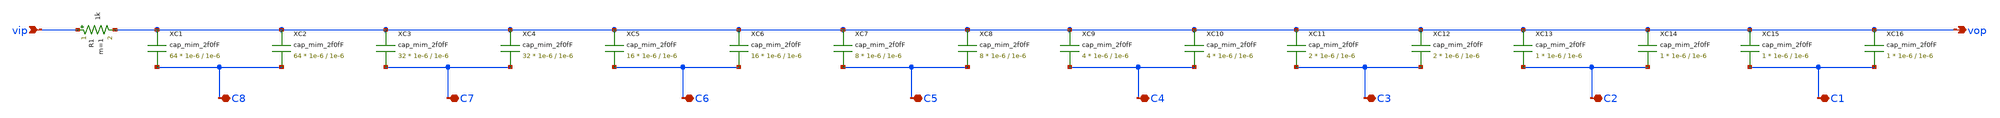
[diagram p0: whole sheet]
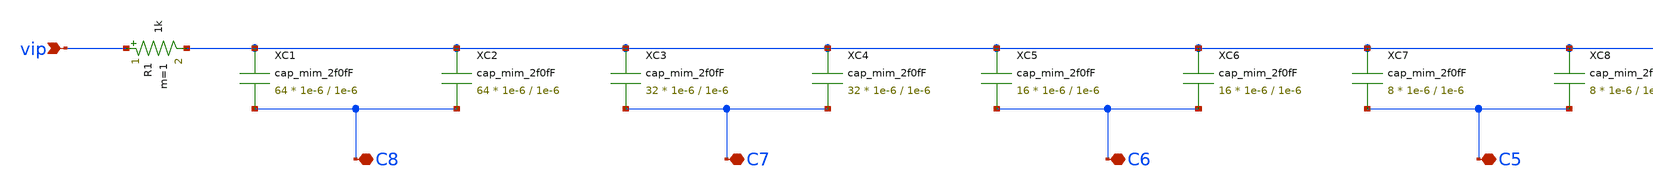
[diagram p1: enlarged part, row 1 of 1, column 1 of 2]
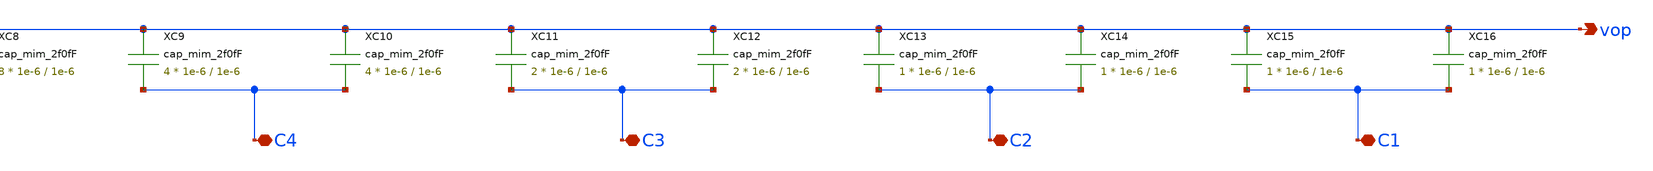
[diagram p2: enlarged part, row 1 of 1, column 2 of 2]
** sch_path: xschem/CDAC.sch
**.subckt CDAC C8 C7 C6 C5 C4 C3 C2 C1 vop vip
*.iopin C8
*.iopin C7
*.iopin C6
*.iopin C5
*.iopin C4
*.iopin C3
*.iopin C2
*.iopin C1
*.opin vop
*.ipin vip
XC1 vop C8 cap_mim_2f0fF c_width=1e-6 c_length=1e-6 m=64
XC2 vop C8 cap_mim_2f0fF c_width=1e-6 c_length=1e-6 m=64
XC3 vop C7 cap_mim_2f0fF c_width=1e-6 c_length=1e-6 m=32
XC4 vop C7 cap_mim_2f0fF c_width=1e-6 c_length=1e-6 m=32
XC5 vop C6 cap_mim_2f0fF c_width=1e-6 c_length=1e-6 m=16
XC6 vop C6 cap_mim_2f0fF c_width=1e-6 c_length=1e-6 m=16
R1 vip vop 1k m=1
XC7 vop C5 cap_mim_2f0fF c_width=1e-6 c_length=1e-6 m=8
XC8 vop C5 cap_mim_2f0fF c_width=1e-6 c_length=1e-6 m=8
XC9 vop C4 cap_mim_2f0fF c_width=1e-6 c_length=1e-6 m=4
XC10 vop C4 cap_mim_2f0fF c_width=1e-6 c_length=1e-6 m=4
XC11 vop C3 cap_mim_2f0fF c_width=1e-6 c_length=1e-6 m=2
XC12 vop C3 cap_mim_2f0fF c_width=1e-6 c_length=1e-6 m=2
XC13 vop C2 cap_mim_2f0fF c_width=1e-6 c_length=1e-6 m=1
XC14 vop C2 cap_mim_2f0fF c_width=1e-6 c_length=1e-6 m=1
XC15 vop C1 cap_mim_2f0fF c_width=1e-6 c_length=1e-6 m=1
XC16 vop C1 cap_mim_2f0fF c_width=1e-6 c_length=1e-6 m=1
**.ends
.end
